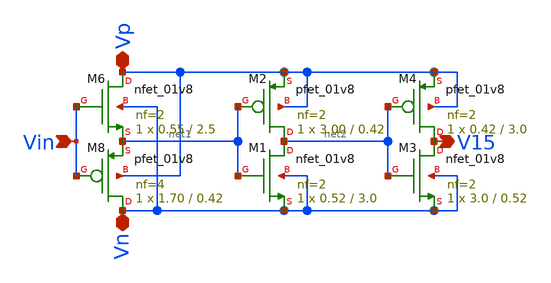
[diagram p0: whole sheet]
** sch_path: xschem/tr1/symbol/th15.sch
**.subckt th15 Vin Vp Vn V15
*.ipin Vin
*.iopin Vp
*.iopin Vn
*.opin V15
XM6 Vp Vin net1 Vn sky130_fd_pr__nfet_01v8 L=2.5 W=0.55 nf=2 ad='int((nf+1)/2) * W/nf * 0.29' as='int((nf+2)/2) * W/nf * 0.29'
+ pd='2*int((nf+1)/2) * (W/nf + 0.29)' ps='2*int((nf+2)/2) * (W/nf + 0.29)' nrd='0.29 / W' nrs='0.29 / W'
+ sa=0 sb=0 sd=0 mult=1 m=1
XM8 Vn Vin net1 Vp sky130_fd_pr__pfet_01v8 L=0.42 W=1.70 nf=4 ad='int((nf+1)/2) * W/nf * 0.29' as='int((nf+2)/2) * W/nf * 0.29'
+ pd='2*int((nf+1)/2) * (W/nf + 0.29)' ps='2*int((nf+2)/2) * (W/nf + 0.29)' nrd='0.29 / W' nrs='0.29 / W'
+ sa=0 sb=0 sd=0 mult=1 m=1
XM1 net2 net1 Vn Vn sky130_fd_pr__nfet_01v8 L=3.0 W=0.52 nf=2 ad='int((nf+1)/2) * W/nf * 0.29' as='int((nf+2)/2) * W/nf * 0.29'
+ pd='2*int((nf+1)/2) * (W/nf + 0.29)' ps='2*int((nf+2)/2) * (W/nf + 0.29)' nrd='0.29 / W' nrs='0.29 / W'
+ sa=0 sb=0 sd=0 mult=1 m=1
XM2 net2 net1 Vp Vp sky130_fd_pr__pfet_01v8 L=0.42 W=3.00 nf=2 ad='int((nf+1)/2) * W/nf * 0.29' as='int((nf+2)/2) * W/nf * 0.29'
+ pd='2*int((nf+1)/2) * (W/nf + 0.29)' ps='2*int((nf+2)/2) * (W/nf + 0.29)' nrd='0.29 / W' nrs='0.29 / W'
+ sa=0 sb=0 sd=0 mult=1 m=1
XM3 V15 net2 Vn Vn sky130_fd_pr__nfet_01v8 L=0.52 W=3.0 nf=2 ad='int((nf+1)/2) * W/nf * 0.29' as='int((nf+2)/2) * W/nf * 0.29'
+ pd='2*int((nf+1)/2) * (W/nf + 0.29)' ps='2*int((nf+2)/2) * (W/nf + 0.29)' nrd='0.29 / W' nrs='0.29 / W'
+ sa=0 sb=0 sd=0 mult=1 m=1
XM4 V15 net2 Vp Vp sky130_fd_pr__pfet_01v8 L=3.0 W=0.42 nf=2 ad='int((nf+1)/2) * W/nf * 0.29' as='int((nf+2)/2) * W/nf * 0.29'
+ pd='2*int((nf+1)/2) * (W/nf + 0.29)' ps='2*int((nf+2)/2) * (W/nf + 0.29)' nrd='0.29 / W' nrs='0.29 / W'
+ sa=0 sb=0 sd=0 mult=1 m=1
**.ends
.end
